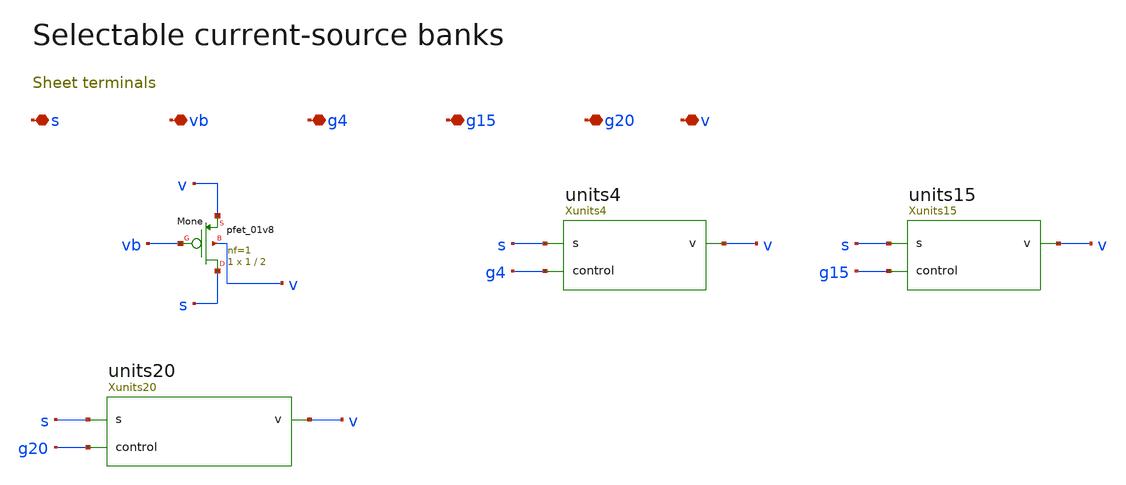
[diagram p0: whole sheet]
** sch_path: review/xschem/tail.sch
**.subckt tail s vb g4 g15 g20 v
*.iopin s
*.iopin vb
*.iopin g4
*.iopin g15
*.iopin g20
*.iopin v
XMone s vb v v sky130_fd_pr__pfet_01v8 L=2 W=1 nf=1 ad='int((nf+1)/2) * W/nf * 0.29' as='int((nf+2)/2) * W/nf * 0.29'
+ pd='2*int((nf+1)/2) * (W/nf + 0.29)' ps='2*int((nf+2)/2) * (W/nf + 0.29)' nrd='0.29 / W' nrs='0.29 / W'
+ sa=0 sb=0 sd=0 mult=1 m=1
Xunits4 s g4 v units4
Xunits15 s g15 v units15
Xunits20 s g20 v units20
**.ends

* expanding   symbol:  units4.sym # of pins=3
** sym_path: review/xschem/units4.sym
** sch_path: review/xschem/units4.sch
.subckt units4 s control v
*.iopin s
*.iopin control
*.iopin v
XMg4_1 s control v v sky130_fd_pr__pfet_01v8 L=2 W=1 nf=1 ad='int((nf+1)/2) * W/nf * 0.29' as='int((nf+2)/2) * W/nf * 0.29'
+ pd='2*int((nf+1)/2) * (W/nf + 0.29)' ps='2*int((nf+2)/2) * (W/nf + 0.29)' nrd='0.29 / W' nrs='0.29 / W'
+ sa=0 sb=0 sd=0 mult=1 m=1
XMg4_2 s control v v sky130_fd_pr__pfet_01v8 L=2 W=1 nf=1 ad='int((nf+1)/2) * W/nf * 0.29' as='int((nf+2)/2) * W/nf * 0.29'
+ pd='2*int((nf+1)/2) * (W/nf + 0.29)' ps='2*int((nf+2)/2) * (W/nf + 0.29)' nrd='0.29 / W' nrs='0.29 / W'
+ sa=0 sb=0 sd=0 mult=1 m=1
XMg4_3 s control v v sky130_fd_pr__pfet_01v8 L=2 W=1 nf=1 ad='int((nf+1)/2) * W/nf * 0.29' as='int((nf+2)/2) * W/nf * 0.29'
+ pd='2*int((nf+1)/2) * (W/nf + 0.29)' ps='2*int((nf+2)/2) * (W/nf + 0.29)' nrd='0.29 / W' nrs='0.29 / W'
+ sa=0 sb=0 sd=0 mult=1 m=1
XMg4_4 s control v v sky130_fd_pr__pfet_01v8 L=2 W=1 nf=1 ad='int((nf+1)/2) * W/nf * 0.29' as='int((nf+2)/2) * W/nf * 0.29'
+ pd='2*int((nf+1)/2) * (W/nf + 0.29)' ps='2*int((nf+2)/2) * (W/nf + 0.29)' nrd='0.29 / W' nrs='0.29 / W'
+ sa=0 sb=0 sd=0 mult=1 m=1
.ends


* expanding   symbol:  units15.sym # of pins=3
** sym_path: review/xschem/units15.sym
** sch_path: review/xschem/units15.sch
.subckt units15 s control v
*.iopin s
*.iopin control
*.iopin v
XMg15_1 s control v v sky130_fd_pr__pfet_01v8 L=2 W=1 nf=1 ad='int((nf+1)/2) * W/nf * 0.29' as='int((nf+2)/2) * W/nf * 0.29'
+ pd='2*int((nf+1)/2) * (W/nf + 0.29)' ps='2*int((nf+2)/2) * (W/nf + 0.29)' nrd='0.29 / W' nrs='0.29 / W'
+ sa=0 sb=0 sd=0 mult=1 m=1
XMg15_2 s control v v sky130_fd_pr__pfet_01v8 L=2 W=1 nf=1 ad='int((nf+1)/2) * W/nf * 0.29' as='int((nf+2)/2) * W/nf * 0.29'
+ pd='2*int((nf+1)/2) * (W/nf + 0.29)' ps='2*int((nf+2)/2) * (W/nf + 0.29)' nrd='0.29 / W' nrs='0.29 / W'
+ sa=0 sb=0 sd=0 mult=1 m=1
XMg15_3 s control v v sky130_fd_pr__pfet_01v8 L=2 W=1 nf=1 ad='int((nf+1)/2) * W/nf * 0.29' as='int((nf+2)/2) * W/nf * 0.29'
+ pd='2*int((nf+1)/2) * (W/nf + 0.29)' ps='2*int((nf+2)/2) * (W/nf + 0.29)' nrd='0.29 / W' nrs='0.29 / W'
+ sa=0 sb=0 sd=0 mult=1 m=1
XMg15_4 s control v v sky130_fd_pr__pfet_01v8 L=2 W=1 nf=1 ad='int((nf+1)/2) * W/nf * 0.29' as='int((nf+2)/2) * W/nf * 0.29'
+ pd='2*int((nf+1)/2) * (W/nf + 0.29)' ps='2*int((nf+2)/2) * (W/nf + 0.29)' nrd='0.29 / W' nrs='0.29 / W'
+ sa=0 sb=0 sd=0 mult=1 m=1
XMg15_5 s control v v sky130_fd_pr__pfet_01v8 L=2 W=1 nf=1 ad='int((nf+1)/2) * W/nf * 0.29' as='int((nf+2)/2) * W/nf * 0.29'
+ pd='2*int((nf+1)/2) * (W/nf + 0.29)' ps='2*int((nf+2)/2) * (W/nf + 0.29)' nrd='0.29 / W' nrs='0.29 / W'
+ sa=0 sb=0 sd=0 mult=1 m=1
XMg15_6 s control v v sky130_fd_pr__pfet_01v8 L=2 W=1 nf=1 ad='int((nf+1)/2) * W/nf * 0.29' as='int((nf+2)/2) * W/nf * 0.29'
+ pd='2*int((nf+1)/2) * (W/nf + 0.29)' ps='2*int((nf+2)/2) * (W/nf + 0.29)' nrd='0.29 / W' nrs='0.29 / W'
+ sa=0 sb=0 sd=0 mult=1 m=1
XMg15_7 s control v v sky130_fd_pr__pfet_01v8 L=2 W=1 nf=1 ad='int((nf+1)/2) * W/nf * 0.29' as='int((nf+2)/2) * W/nf * 0.29'
+ pd='2*int((nf+1)/2) * (W/nf + 0.29)' ps='2*int((nf+2)/2) * (W/nf + 0.29)' nrd='0.29 / W' nrs='0.29 / W'
+ sa=0 sb=0 sd=0 mult=1 m=1
XMg15_8 s control v v sky130_fd_pr__pfet_01v8 L=2 W=1 nf=1 ad='int((nf+1)/2) * W/nf * 0.29' as='int((nf+2)/2) * W/nf * 0.29'
+ pd='2*int((nf+1)/2) * (W/nf + 0.29)' ps='2*int((nf+2)/2) * (W/nf + 0.29)' nrd='0.29 / W' nrs='0.29 / W'
+ sa=0 sb=0 sd=0 mult=1 m=1
XMg15_9 s control v v sky130_fd_pr__pfet_01v8 L=2 W=1 nf=1 ad='int((nf+1)/2) * W/nf * 0.29' as='int((nf+2)/2) * W/nf * 0.29'
+ pd='2*int((nf+1)/2) * (W/nf + 0.29)' ps='2*int((nf+2)/2) * (W/nf + 0.29)' nrd='0.29 / W' nrs='0.29 / W'
+ sa=0 sb=0 sd=0 mult=1 m=1
XMg15_10 s control v v sky130_fd_pr__pfet_01v8 L=2 W=1 nf=1 ad='int((nf+1)/2) * W/nf * 0.29' as='int((nf+2)/2) * W/nf * 0.29'
+ pd='2*int((nf+1)/2) * (W/nf + 0.29)' ps='2*int((nf+2)/2) * (W/nf + 0.29)' nrd='0.29 / W' nrs='0.29 / W'
+ sa=0 sb=0 sd=0 mult=1 m=1
XMg15_11 s control v v sky130_fd_pr__pfet_01v8 L=2 W=1 nf=1 ad='int((nf+1)/2) * W/nf * 0.29' as='int((nf+2)/2) * W/nf * 0.29'
+ pd='2*int((nf+1)/2) * (W/nf + 0.29)' ps='2*int((nf+2)/2) * (W/nf + 0.29)' nrd='0.29 / W' nrs='0.29 / W'
+ sa=0 sb=0 sd=0 mult=1 m=1
XMg15_12 s control v v sky130_fd_pr__pfet_01v8 L=2 W=1 nf=1 ad='int((nf+1)/2) * W/nf * 0.29' as='int((nf+2)/2) * W/nf * 0.29'
+ pd='2*int((nf+1)/2) * (W/nf + 0.29)' ps='2*int((nf+2)/2) * (W/nf + 0.29)' nrd='0.29 / W' nrs='0.29 / W'
+ sa=0 sb=0 sd=0 mult=1 m=1
XMg15_13 s control v v sky130_fd_pr__pfet_01v8 L=2 W=1 nf=1 ad='int((nf+1)/2) * W/nf * 0.29' as='int((nf+2)/2) * W/nf * 0.29'
+ pd='2*int((nf+1)/2) * (W/nf + 0.29)' ps='2*int((nf+2)/2) * (W/nf + 0.29)' nrd='0.29 / W' nrs='0.29 / W'
+ sa=0 sb=0 sd=0 mult=1 m=1
XMg15_14 s control v v sky130_fd_pr__pfet_01v8 L=2 W=1 nf=1 ad='int((nf+1)/2) * W/nf * 0.29' as='int((nf+2)/2) * W/nf * 0.29'
+ pd='2*int((nf+1)/2) * (W/nf + 0.29)' ps='2*int((nf+2)/2) * (W/nf + 0.29)' nrd='0.29 / W' nrs='0.29 / W'
+ sa=0 sb=0 sd=0 mult=1 m=1
XMg15_15 s control v v sky130_fd_pr__pfet_01v8 L=2 W=1 nf=1 ad='int((nf+1)/2) * W/nf * 0.29' as='int((nf+2)/2) * W/nf * 0.29'
+ pd='2*int((nf+1)/2) * (W/nf + 0.29)' ps='2*int((nf+2)/2) * (W/nf + 0.29)' nrd='0.29 / W' nrs='0.29 / W'
+ sa=0 sb=0 sd=0 mult=1 m=1
.ends


* expanding   symbol:  units20.sym # of pins=3
** sym_path: review/xschem/units20.sym
** sch_path: review/xschem/units20.sch
.subckt units20 s control v
*.iopin s
*.iopin control
*.iopin v
XMg20_1 s control v v sky130_fd_pr__pfet_01v8 L=2 W=1 nf=1 ad='int((nf+1)/2) * W/nf * 0.29' as='int((nf+2)/2) * W/nf * 0.29'
+ pd='2*int((nf+1)/2) * (W/nf + 0.29)' ps='2*int((nf+2)/2) * (W/nf + 0.29)' nrd='0.29 / W' nrs='0.29 / W'
+ sa=0 sb=0 sd=0 mult=1 m=1
XMg20_2 s control v v sky130_fd_pr__pfet_01v8 L=2 W=1 nf=1 ad='int((nf+1)/2) * W/nf * 0.29' as='int((nf+2)/2) * W/nf * 0.29'
+ pd='2*int((nf+1)/2) * (W/nf + 0.29)' ps='2*int((nf+2)/2) * (W/nf + 0.29)' nrd='0.29 / W' nrs='0.29 / W'
+ sa=0 sb=0 sd=0 mult=1 m=1
XMg20_3 s control v v sky130_fd_pr__pfet_01v8 L=2 W=1 nf=1 ad='int((nf+1)/2) * W/nf * 0.29' as='int((nf+2)/2) * W/nf * 0.29'
+ pd='2*int((nf+1)/2) * (W/nf + 0.29)' ps='2*int((nf+2)/2) * (W/nf + 0.29)' nrd='0.29 / W' nrs='0.29 / W'
+ sa=0 sb=0 sd=0 mult=1 m=1
XMg20_4 s control v v sky130_fd_pr__pfet_01v8 L=2 W=1 nf=1 ad='int((nf+1)/2) * W/nf * 0.29' as='int((nf+2)/2) * W/nf * 0.29'
+ pd='2*int((nf+1)/2) * (W/nf + 0.29)' ps='2*int((nf+2)/2) * (W/nf + 0.29)' nrd='0.29 / W' nrs='0.29 / W'
+ sa=0 sb=0 sd=0 mult=1 m=1
XMg20_5 s control v v sky130_fd_pr__pfet_01v8 L=2 W=1 nf=1 ad='int((nf+1)/2) * W/nf * 0.29' as='int((nf+2)/2) * W/nf * 0.29'
+ pd='2*int((nf+1)/2) * (W/nf + 0.29)' ps='2*int((nf+2)/2) * (W/nf + 0.29)' nrd='0.29 / W' nrs='0.29 / W'
+ sa=0 sb=0 sd=0 mult=1 m=1
XMg20_6 s control v v sky130_fd_pr__pfet_01v8 L=2 W=1 nf=1 ad='int((nf+1)/2) * W/nf * 0.29' as='int((nf+2)/2) * W/nf * 0.29'
+ pd='2*int((nf+1)/2) * (W/nf + 0.29)' ps='2*int((nf+2)/2) * (W/nf + 0.29)' nrd='0.29 / W' nrs='0.29 / W'
+ sa=0 sb=0 sd=0 mult=1 m=1
XMg20_7 s control v v sky130_fd_pr__pfet_01v8 L=2 W=1 nf=1 ad='int((nf+1)/2) * W/nf * 0.29' as='int((nf+2)/2) * W/nf * 0.29'
+ pd='2*int((nf+1)/2) * (W/nf + 0.29)' ps='2*int((nf+2)/2) * (W/nf + 0.29)' nrd='0.29 / W' nrs='0.29 / W'
+ sa=0 sb=0 sd=0 mult=1 m=1
XMg20_8 s control v v sky130_fd_pr__pfet_01v8 L=2 W=1 nf=1 ad='int((nf+1)/2) * W/nf * 0.29' as='int((nf+2)/2) * W/nf * 0.29'
+ pd='2*int((nf+1)/2) * (W/nf + 0.29)' ps='2*int((nf+2)/2) * (W/nf + 0.29)' nrd='0.29 / W' nrs='0.29 / W'
+ sa=0 sb=0 sd=0 mult=1 m=1
XMg20_9 s control v v sky130_fd_pr__pfet_01v8 L=2 W=1 nf=1 ad='int((nf+1)/2) * W/nf * 0.29' as='int((nf+2)/2) * W/nf * 0.29'
+ pd='2*int((nf+1)/2) * (W/nf + 0.29)' ps='2*int((nf+2)/2) * (W/nf + 0.29)' nrd='0.29 / W' nrs='0.29 / W'
+ sa=0 sb=0 sd=0 mult=1 m=1
XMg20_10 s control v v sky130_fd_pr__pfet_01v8 L=2 W=1 nf=1 ad='int((nf+1)/2) * W/nf * 0.29' as='int((nf+2)/2) * W/nf * 0.29'
+ pd='2*int((nf+1)/2) * (W/nf + 0.29)' ps='2*int((nf+2)/2) * (W/nf + 0.29)' nrd='0.29 / W' nrs='0.29 / W'
+ sa=0 sb=0 sd=0 mult=1 m=1
XMg20_11 s control v v sky130_fd_pr__pfet_01v8 L=2 W=1 nf=1 ad='int((nf+1)/2) * W/nf * 0.29' as='int((nf+2)/2) * W/nf * 0.29'
+ pd='2*int((nf+1)/2) * (W/nf + 0.29)' ps='2*int((nf+2)/2) * (W/nf + 0.29)' nrd='0.29 / W' nrs='0.29 / W'
+ sa=0 sb=0 sd=0 mult=1 m=1
XMg20_12 s control v v sky130_fd_pr__pfet_01v8 L=2 W=1 nf=1 ad='int((nf+1)/2) * W/nf * 0.29' as='int((nf+2)/2) * W/nf * 0.29'
+ pd='2*int((nf+1)/2) * (W/nf + 0.29)' ps='2*int((nf+2)/2) * (W/nf + 0.29)' nrd='0.29 / W' nrs='0.29 / W'
+ sa=0 sb=0 sd=0 mult=1 m=1
XMg20_13 s control v v sky130_fd_pr__pfet_01v8 L=2 W=1 nf=1 ad='int((nf+1)/2) * W/nf * 0.29' as='int((nf+2)/2) * W/nf * 0.29'
+ pd='2*int((nf+1)/2) * (W/nf + 0.29)' ps='2*int((nf+2)/2) * (W/nf + 0.29)' nrd='0.29 / W' nrs='0.29 / W'
+ sa=0 sb=0 sd=0 mult=1 m=1
XMg20_14 s control v v sky130_fd_pr__pfet_01v8 L=2 W=1 nf=1 ad='int((nf+1)/2) * W/nf * 0.29' as='int((nf+2)/2) * W/nf * 0.29'
+ pd='2*int((nf+1)/2) * (W/nf + 0.29)' ps='2*int((nf+2)/2) * (W/nf + 0.29)' nrd='0.29 / W' nrs='0.29 / W'
+ sa=0 sb=0 sd=0 mult=1 m=1
XMg20_15 s control v v sky130_fd_pr__pfet_01v8 L=2 W=1 nf=1 ad='int((nf+1)/2) * W/nf * 0.29' as='int((nf+2)/2) * W/nf * 0.29'
+ pd='2*int((nf+1)/2) * (W/nf + 0.29)' ps='2*int((nf+2)/2) * (W/nf + 0.29)' nrd='0.29 / W' nrs='0.29 / W'
+ sa=0 sb=0 sd=0 mult=1 m=1
XMg20_16 s control v v sky130_fd_pr__pfet_01v8 L=2 W=1 nf=1 ad='int((nf+1)/2) * W/nf * 0.29' as='int((nf+2)/2) * W/nf * 0.29'
+ pd='2*int((nf+1)/2) * (W/nf + 0.29)' ps='2*int((nf+2)/2) * (W/nf + 0.29)' nrd='0.29 / W' nrs='0.29 / W'
+ sa=0 sb=0 sd=0 mult=1 m=1
XMg20_17 s control v v sky130_fd_pr__pfet_01v8 L=2 W=1 nf=1 ad='int((nf+1)/2) * W/nf * 0.29' as='int((nf+2)/2) * W/nf * 0.29'
+ pd='2*int((nf+1)/2) * (W/nf + 0.29)' ps='2*int((nf+2)/2) * (W/nf + 0.29)' nrd='0.29 / W' nrs='0.29 / W'
+ sa=0 sb=0 sd=0 mult=1 m=1
XMg20_18 s control v v sky130_fd_pr__pfet_01v8 L=2 W=1 nf=1 ad='int((nf+1)/2) * W/nf * 0.29' as='int((nf+2)/2) * W/nf * 0.29'
+ pd='2*int((nf+1)/2) * (W/nf + 0.29)' ps='2*int((nf+2)/2) * (W/nf + 0.29)' nrd='0.29 / W' nrs='0.29 / W'
+ sa=0 sb=0 sd=0 mult=1 m=1
XMg20_19 s control v v sky130_fd_pr__pfet_01v8 L=2 W=1 nf=1 ad='int((nf+1)/2) * W/nf * 0.29' as='int((nf+2)/2) * W/nf * 0.29'
+ pd='2*int((nf+1)/2) * (W/nf + 0.29)' ps='2*int((nf+2)/2) * (W/nf + 0.29)' nrd='0.29 / W' nrs='0.29 / W'
+ sa=0 sb=0 sd=0 mult=1 m=1
XMg20_20 s control v v sky130_fd_pr__pfet_01v8 L=2 W=1 nf=1 ad='int((nf+1)/2) * W/nf * 0.29' as='int((nf+2)/2) * W/nf * 0.29'
+ pd='2*int((nf+1)/2) * (W/nf + 0.29)' ps='2*int((nf+2)/2) * (W/nf + 0.29)' nrd='0.29 / W' nrs='0.29 / W'
+ sa=0 sb=0 sd=0 mult=1 m=1
.ends

.end
